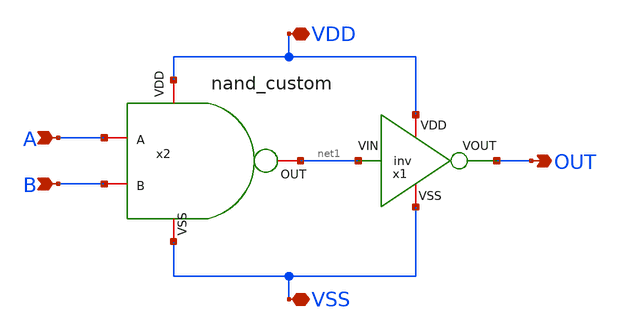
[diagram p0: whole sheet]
** sch_path: design/blocks-std-custom/and_custom/schematic/and_custom.sch
**.subckt and_custom A VDD OUT VSS B
*.ipin A
*.iopin VDD
*.opin OUT
*.iopin VSS
*.ipin B
x1 VDD OUT net1 VSS inv
x2 VDD net1 A B VSS nand_custom
**.ends

* expanding   symbol:  blocks-std-custom/nand_custom/schematic/nand_custom.sym # of pins=5
** sym_path: Custom_std_cells/nand_custom.sym
** sch_path: Custom_std_cells/nand_custom.sch
.subckt nand_custom VDD OUT A B VSS
*.iopin VDD
*.iopin VSS
*.ipin A
*.ipin B
*.opin OUT
XM1 OUT A net1 VSS sg13_lv_nmos w=0.15u l=0.13u ng=1 m=1 mm_ok=1
XM2 OUT A VDD VDD sg13_lv_pmos w=0.15u l=0.13u ng=1 m=1 mm_ok=1
XM3 net1 B VSS VSS sg13_lv_nmos w=0.15u l=0.13u ng=1 m=1 mm_ok=1
XM4 OUT B VDD VDD sg13_lv_pmos w=0.15u l=0.13u ng=1 m=1 mm_ok=1
.ends

.end
